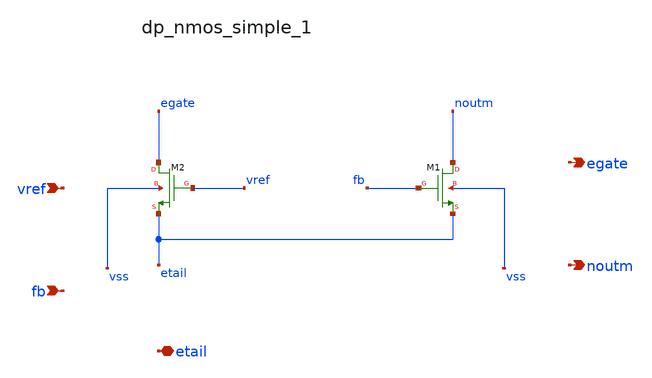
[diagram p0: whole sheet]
** sch_path: analog-db/raw/ldo_007_pmos/hier/blocks/dp_nmos_simple_1.sch
**.subckt dp_nmos_simple_1 vref fb etail egate noutm
*.ipin vref
*.ipin fb
*.iopin etail
*.opin egate
*.opin noutm
XM1 noutm fb etail vss sg13_lv_nmos w=x_dut_xm1_w l=x_dut_xm1_l ng=1 m=1
XM2 egate vref etail vss sg13_lv_nmos w=x_dut_xm2_w l=x_dut_xm2_l ng=1 m=1
**.ends
.end
